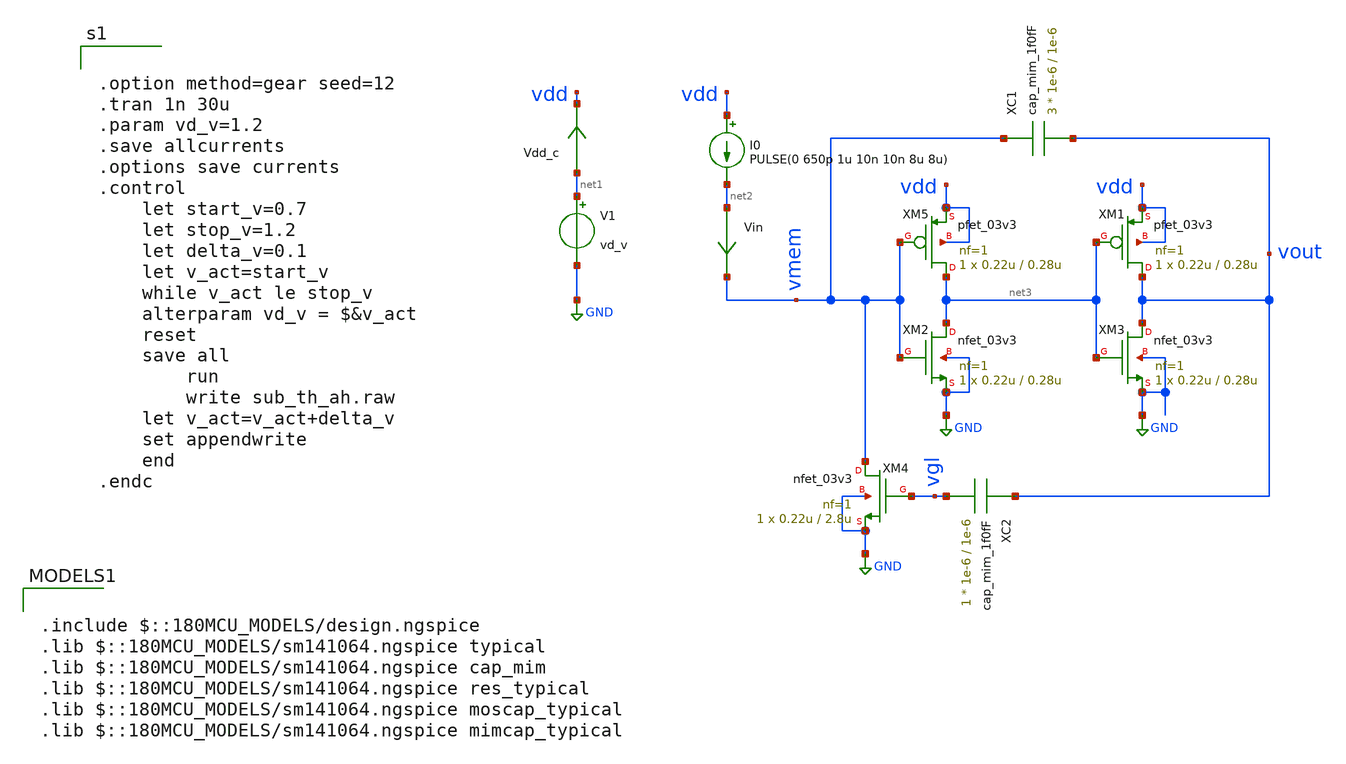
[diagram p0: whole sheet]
** sch_path: designs_testing/libs/core_AH_neuron/AH_neuron.sch
**.subckt AH_neuron
V1 net1 GND vd_v
Vdd_c net1 vdd 0
.save i(vdd_c)
I0 vdd net2 PULSE(0 650p 1u 10n 10n 8u 8u)
Vin net2 vmem 0
.save i(vin)
XM5 net3 vmem vdd vdd pfet_03v3 L=0.28u W=0.22u nf=1 ad='int((nf+1)/2) * W/nf * 0.18u' as='int((nf+2)/2) * W/nf * 0.18u'
+ pd='2*int((nf+1)/2) * (W/nf + 0.18u)' ps='2*int((nf+2)/2) * (W/nf + 0.18u)' nrd='0.18u / W' nrs='0.18u / W'
+ sa=0 sb=0 sd=0 m=1
XM1 vout net3 vdd vdd pfet_03v3 L=0.28u W=0.22u nf=1 ad='int((nf+1)/2) * W/nf * 0.18u' as='int((nf+2)/2) * W/nf * 0.18u'
+ pd='2*int((nf+1)/2) * (W/nf + 0.18u)' ps='2*int((nf+2)/2) * (W/nf + 0.18u)' nrd='0.18u / W' nrs='0.18u / W'
+ sa=0 sb=0 sd=0 m=1
XM2 net3 vmem GND GND nfet_03v3 L=0.28u W=0.22u nf=1 ad='int((nf+1)/2) * W/nf * 0.18u' as='int((nf+2)/2) * W/nf * 0.18u'
+ pd='2*int((nf+1)/2) * (W/nf + 0.18u)' ps='2*int((nf+2)/2) * (W/nf + 0.18u)' nrd='0.18u / W' nrs='0.18u / W'
+ sa=0 sb=0 sd=0 m=1
XM3 vout net3 GND GND nfet_03v3 L=0.28u W=0.22u nf=1 ad='int((nf+1)/2) * W/nf * 0.18u' as='int((nf+2)/2) * W/nf * 0.18u'
+ pd='2*int((nf+1)/2) * (W/nf + 0.18u)' ps='2*int((nf+2)/2) * (W/nf + 0.18u)' nrd='0.18u / W' nrs='0.18u / W'
+ sa=0 sb=0 sd=0 m=1
XM4 vmem vgl GND GND nfet_03v3 L=2.8u W=0.22u nf=1 ad='int((nf+1)/2) * W/nf * 0.18u' as='int((nf+2)/2) * W/nf * 0.18u'
+ pd='2*int((nf+1)/2) * (W/nf + 0.18u)' ps='2*int((nf+2)/2) * (W/nf + 0.18u)' nrd='0.18u / W' nrs='0.18u / W'
+ sa=0 sb=0 sd=0 m=1
XC1 vmem vout cap_mim_1f0fF c_width=1e-6 c_length=1e-6 m=3
XC2 vout vgl cap_mim_1f0fF c_width=1e-6 c_length=1e-6 m=1
**** begin user architecture code


.option method=gear seed=12
.tran 1n 30u
.param vd_v=1.2
.save allcurrents
.options save currents
.control
    let start_v=0.7
    let stop_v=1.2
    let delta_v=0.1
    let v_act=start_v
    while v_act le stop_v
	alterparam vd_v = $&v_act
	reset
	save all
        run
        write sub_th_ah.raw
	let v_act=v_act+delta_v
	set appendwrite
    end
.endc



.include $::180MCU_MODELS/design.ngspice
.lib $::180MCU_MODELS/sm141064.ngspice typical
.lib $::180MCU_MODELS/sm141064.ngspice cap_mim
.lib $::180MCU_MODELS/sm141064.ngspice res_typical
.lib $::180MCU_MODELS/sm141064.ngspice moscap_typical
.lib $::180MCU_MODELS/sm141064.ngspice mimcap_typical

**** end user architecture code
**.ends
.GLOBAL GND
.end
